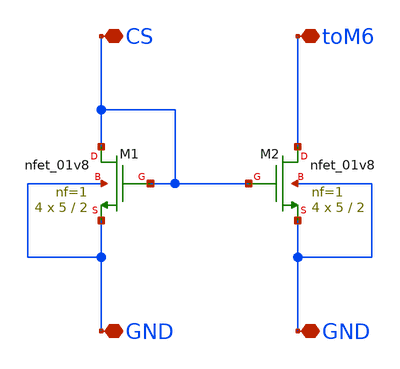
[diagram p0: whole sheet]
** sch_path: mag/NMOS__Current_Mirror_part_LVS.sch
**.subckt NMOS__Current_Mirror_part_LVS CS toM6 GND GND
*.iopin CS
*.iopin toM6
*.iopin GND
*.iopin GND
XM1 CS CS GND GND sky130_fd_pr__nfet_01v8 L=2 W=5 nf=1 ad='int((1 + 1)/2) * 5 / 1 * 0.29' as='int((1 + 2)/2) * 5 / 1 * 0.29'
+ pd='2*int((1 + 1)/2) * (5 / 1 + 0.29)' ps='2*int((1 + 2)/2) * (5 / 1 + 0.29)' nrd='0.29 / 5 ' nrs='0.29 / 5 '
+ sa=0 sb=0 sd=0 mult=4 m=4
XM2 toM6 CS GND GND sky130_fd_pr__nfet_01v8 L=2 W=5 nf=1 ad='int((1 + 1)/2) * 5 / 1 * 0.29' as='int((1 + 2)/2) * 5 / 1 * 0.29'
+ pd='2*int((1 + 1)/2) * (5 / 1 + 0.29)' ps='2*int((1 + 2)/2) * (5 / 1 + 0.29)' nrd='0.29 / 5 ' nrs='0.29 / 5 '
+ sa=0 sb=0 sd=0 mult=4 m=4
**.ends
.end
